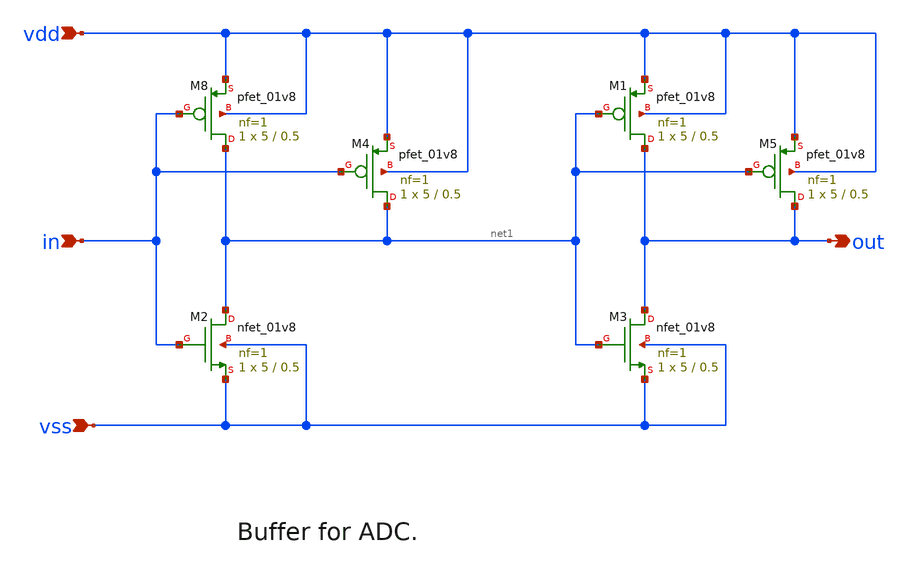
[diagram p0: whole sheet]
** sch_path: xschem/adc_drv.sch
**.subckt adc_drv vdd vss in out
*.ipin vdd
*.ipin vss
*.ipin in
*.opin out
XM2 net1 in vss vss sky130_fd_pr__nfet_01v8 L=0.5 W=5 nf=1 ad='int((nf+1)/2) * W/nf * 0.29' as='int((nf+2)/2) * W/nf * 0.29'
+ pd='2*int((nf+1)/2) * (W/nf + 0.29)' ps='2*int((nf+2)/2) * (W/nf + 0.29)' nrd='0.29 / W' nrs='0.29 / W'
+ sa=0 sb=0 sd=0 mult=1 m=1
XM8 net1 in vdd vdd sky130_fd_pr__pfet_01v8 L=0.5 W=5 nf=1 ad='int((nf+1)/2) * W/nf * 0.29' as='int((nf+2)/2) * W/nf * 0.29'
+ pd='2*int((nf+1)/2) * (W/nf + 0.29)' ps='2*int((nf+2)/2) * (W/nf + 0.29)' nrd='0.29 / W' nrs='0.29 / W'
+ sa=0 sb=0 sd=0 mult=1 m=1
XM1 out net1 vdd vdd sky130_fd_pr__pfet_01v8 L=0.5 W=5 nf=1 ad='int((nf+1)/2) * W/nf * 0.29' as='int((nf+2)/2) * W/nf * 0.29'
+ pd='2*int((nf+1)/2) * (W/nf + 0.29)' ps='2*int((nf+2)/2) * (W/nf + 0.29)' nrd='0.29 / W' nrs='0.29 / W'
+ sa=0 sb=0 sd=0 mult=1 m=1
XM3 out net1 vss vss sky130_fd_pr__nfet_01v8 L=0.5 W=5 nf=1 ad='int((nf+1)/2) * W/nf * 0.29' as='int((nf+2)/2) * W/nf * 0.29'
+ pd='2*int((nf+1)/2) * (W/nf + 0.29)' ps='2*int((nf+2)/2) * (W/nf + 0.29)' nrd='0.29 / W' nrs='0.29 / W'
+ sa=0 sb=0 sd=0 mult=1 m=1
XM4 net1 in vdd vdd sky130_fd_pr__pfet_01v8 L=0.5 W=5 nf=1 ad='int((nf+1)/2) * W/nf * 0.29' as='int((nf+2)/2) * W/nf * 0.29'
+ pd='2*int((nf+1)/2) * (W/nf + 0.29)' ps='2*int((nf+2)/2) * (W/nf + 0.29)' nrd='0.29 / W' nrs='0.29 / W'
+ sa=0 sb=0 sd=0 mult=1 m=1
XM5 out net1 vdd vdd sky130_fd_pr__pfet_01v8 L=0.5 W=5 nf=1 ad='int((nf+1)/2) * W/nf * 0.29' as='int((nf+2)/2) * W/nf * 0.29'
+ pd='2*int((nf+1)/2) * (W/nf + 0.29)' ps='2*int((nf+2)/2) * (W/nf + 0.29)' nrd='0.29 / W' nrs='0.29 / W'
+ sa=0 sb=0 sd=0 mult=1 m=1
**.ends
.end
